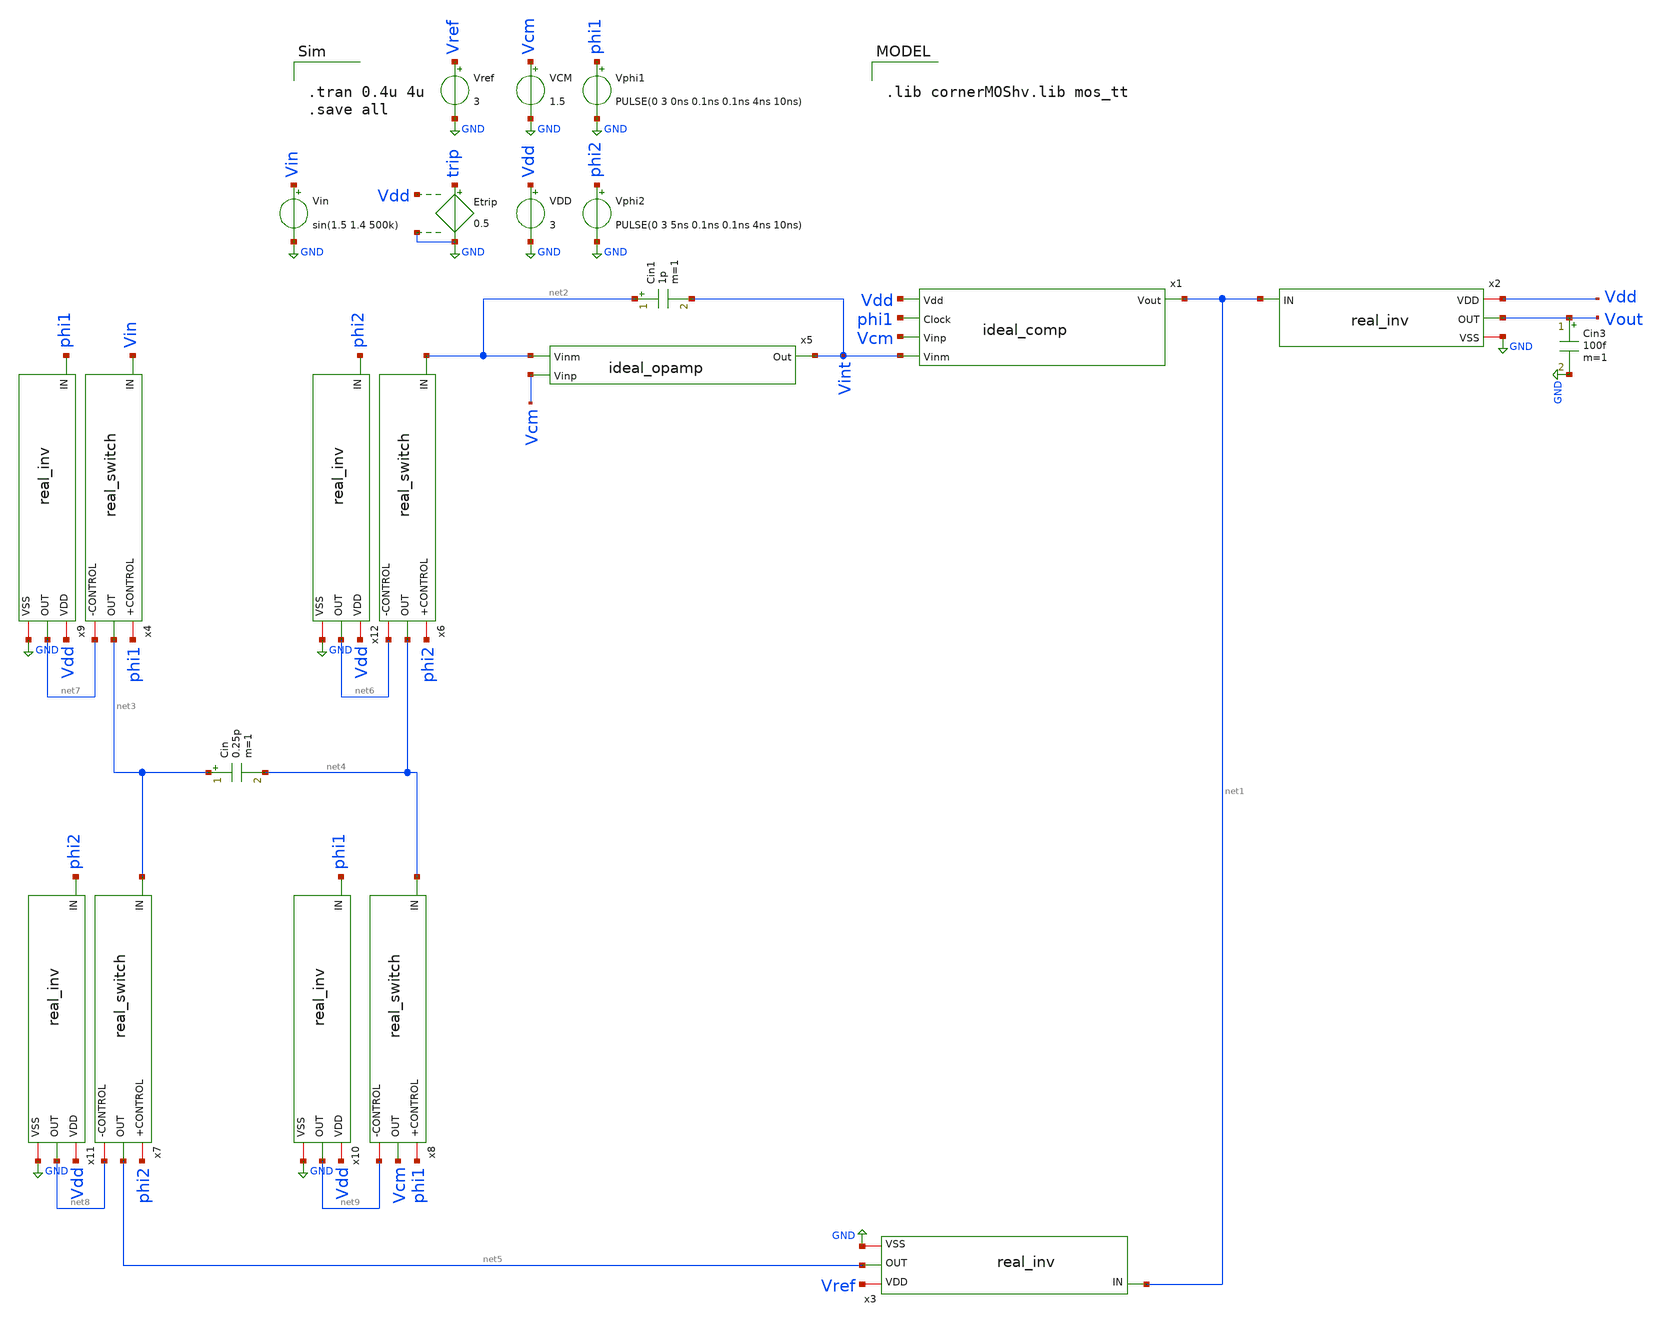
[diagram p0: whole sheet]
** sch_path: real_circuit/real_circuit.sch
**.subckt real_circuit
Etrip trip GND Vdd GND 0.5
Vref Vref GND 3
VDD Vdd GND 3
VCM Vcm GND 1.5
Vin Vin GND sin(1.5 1.4 500k)
Vphi1 phi1 GND PULSE(0 3 0ns 0.1ns 0.1ns 4ns 10ns)
Vphi2 phi2 GND PULSE(0 3 5ns 0.1ns 0.1ns 4ns 10ns)
Cin1 net2 Vint 1p m=1
x5 Vint net2 Vcm ideal_opamp
x1 net1 Vdd phi1 Vcm Vint ideal_comp
x3 Vref net1 net5 GND real_inv
x2 Vdd net1 Vout GND real_inv
Cin net3 net4 0.25p m=1
x4 phi1 Vin net3 net7 real_switch
x6 phi2 net2 net4 net6 real_switch
x7 phi2 net3 net5 net8 real_switch
x8 phi1 net4 Vcm net9 real_switch
x9 Vdd phi1 net7 GND real_inv
x10 Vdd phi1 net9 GND real_inv
x11 Vdd phi2 net8 GND real_inv
x12 Vdd phi2 net6 GND real_inv
Cin3 Vout GND 100f m=1
**** begin user architecture code


.tran 0.4u 4u
.save all



.lib cornerMOShv.lib mos_tt

**** end user architecture code
**.ends
.GLOBAL GND
.end
